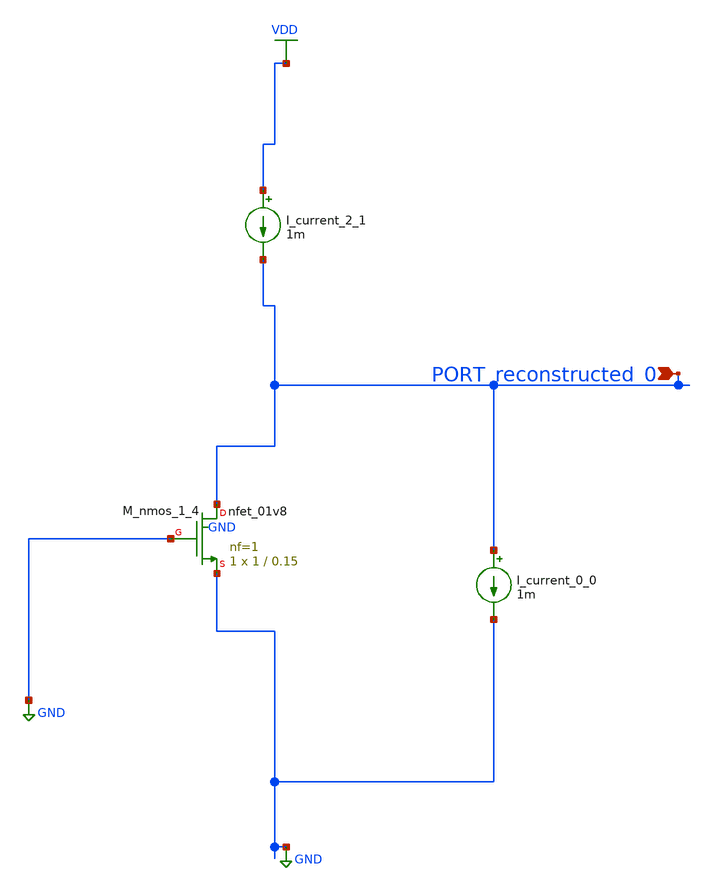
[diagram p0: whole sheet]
** sch_path: schematics/AMSNet/434.sch
**.subckt 434 PORT_reconstructed_0
*.ipin PORT_reconstructed_0
I_current_0_0 PORT_reconstructed_0 GND 1m
I_current_2_1 VDD PORT_reconstructed_0 1m
XM_nmos_1_4 PORT_reconstructed_0 GND GND GND sky130_fd_pr__nfet_01v8 L=0.15 W=1 nf=1 ad='int((1 + 1)/2) * 1 / 1 * 0.29'
+ as='int((1 + 2)/2) * 1 / 1 * 0.29' pd='2*int((1 + 1)/2) * (1 / 1 + 0.29)' ps='2*int((1 + 2)/2) * (1 / 1 + 0.29)'
+ nrd='0.29 / 1 ' nrs='0.29 / 1 ' sa=0 sb=0 sd=0 mult=1 m=1
**.ends
.GLOBAL GND
.GLOBAL VDD
.end
